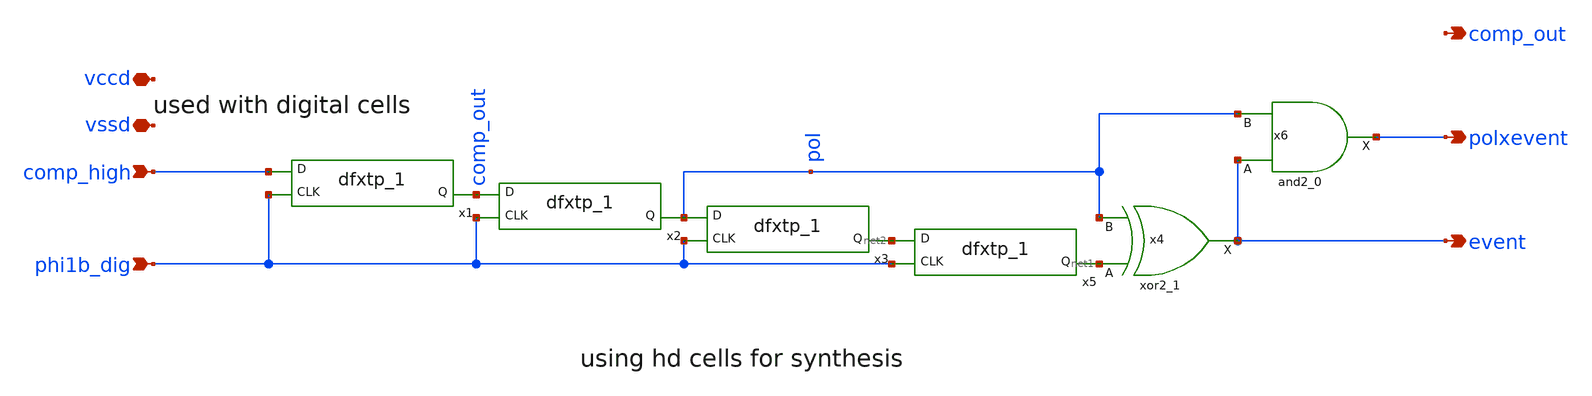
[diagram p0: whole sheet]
** sch_path: xschem/digital/dig_evegen.sch
**.subckt dig_evegen phi1b_dig event comp_out polxevent comp_high vccd vssd
*.ipin phi1b_dig
*.opin event
*.opin comp_out
*.opin polxevent
*.ipin comp_high
*.iopin vccd
*.iopin vssd
x4 net1 pol vssd vssd vccd vccd event sky130_fd_sc_hd__xor2_1
x1 phi1b_dig comp_high vssd vssd vccd vccd comp_out sky130_fd_sc_hd__dfxtp_1
x6 event pol vssd vssd vccd vccd polxevent sky130_fd_sc_hd__and2_0
x2 phi1b_dig comp_out vssd vssd vccd vccd pol sky130_fd_sc_hd__dfxtp_1
x3 phi1b_dig pol vssd vssd vccd vccd net2 sky130_fd_sc_hd__dfxtp_1
x5 phi1b_dig net2 vssd vssd vccd vccd net1 sky130_fd_sc_hd__dfxtp_1
**.ends
.end
